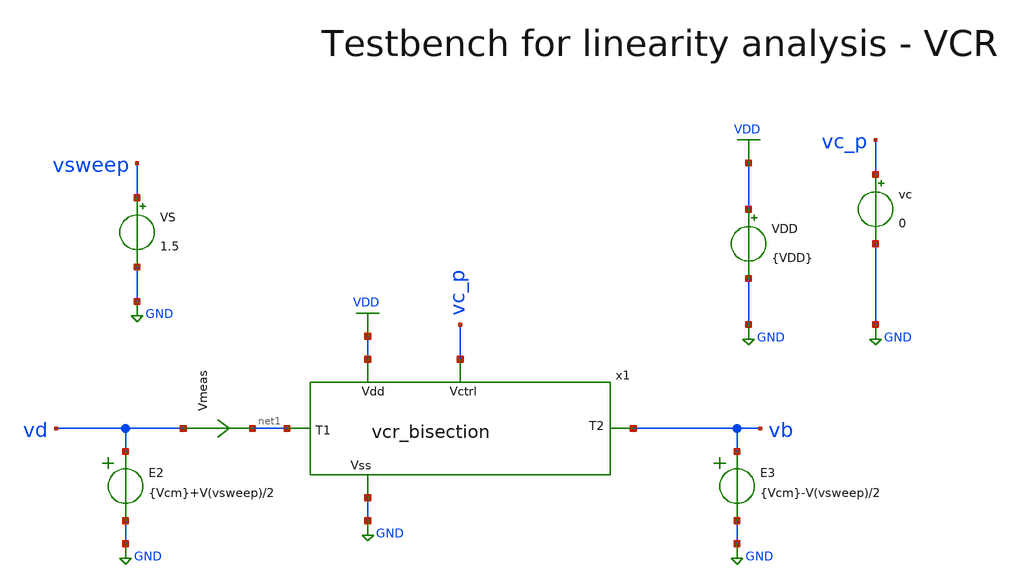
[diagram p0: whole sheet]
** sch_path: macros/voltage_controlled_resistors/macros/vcr_bisection/testbenches/xschem/res_tb_linearity.sch
**.subckt res_tb_linearity
VDD VDD GND {VDD}
VS vsweep GND 1.5
Vmeas vd net1 0
.save i(vmeas)
E2 vd GND VOL=' {Vcm}+V(vsweep)/2 '
E3 vb GND VOL=' {Vcm}-V(vsweep)/2 '
vc vc_p GND 0
x1 vc_p net1 vb VDD GND vcr_bisection
**** begin user architecture code

.lib cornerMOSlv.lib mos_tt
.lib cornerMOShv.lib mos_tt
.lib cornerRES.lib res_typ
.lib cornerDIO.lib dio_tt
.lib cornerCAP.lib cap_typ



* .include ../../../netlist/pex/inverter_magic_pex_3.spice
.param VDD=3.3
.csparam VDD=VDD
.param Vcm=2
.csparam Vcm=Vcm
.param temp=27
.options savecurrents klu method=gear reltol=1e-3 abstol=1e-15 gmin=1e-15 rshunt=1e13
.control
let vcc = 0.75

save all
set appendwrite



repeat 5
  alter vc $&vcc

  * DC Sweep
  dc VS -0.7 0.7 1m
  remzerovec
  let vcc = vcc + 0.25
end
write @schname\.raw
set appendwrite

* Plotting
plot dc1.v(vsweep)/(dc1.v.x1.Vmeas#branch) dc2.v(vsweep)/(dc2.v.x1.Vmeas#branch)
+ dc3.v(vsweep)/(dc3.v.x1.Vmeas#branch) dc4.v(vsweep)/(dc4.v.x1.Vmeas#branch) dc5.v(vsweep)/(dc5.v.x1.Vmeas#branch) ylimit 0 15k

plot dc1.v.x1.Vmeas#branch dc2.v.x1.Vmeas#branch dc3.v.x1.Vmeas#branch dc4.v.x1.Vmeas#branch
+ dc5.v.x1.Vmeas#branch

* Write Data
unset appendwrite
set wr_vecnames
set wr_singlescale
wrdata ../plot_simulations/data/@schname\.txt v(vc_p) dc1.v(vsweep)/(dc1.i(Vmeas))
+ dc2.v(vsweep)/(dc2.i(Vmeas)) dc3.v(vsweep)/(dc3.i(Vmeas)) dc4.v(vsweep)/(dc4.i(Vmeas)) dc5.v(vsweep)/(dc5.i(Vmeas))

write res_tb_linearity.raw

*quit
.endc


**** end user architecture code
**.ends
.GLOBAL GND
.GLOBAL VDD
.end
